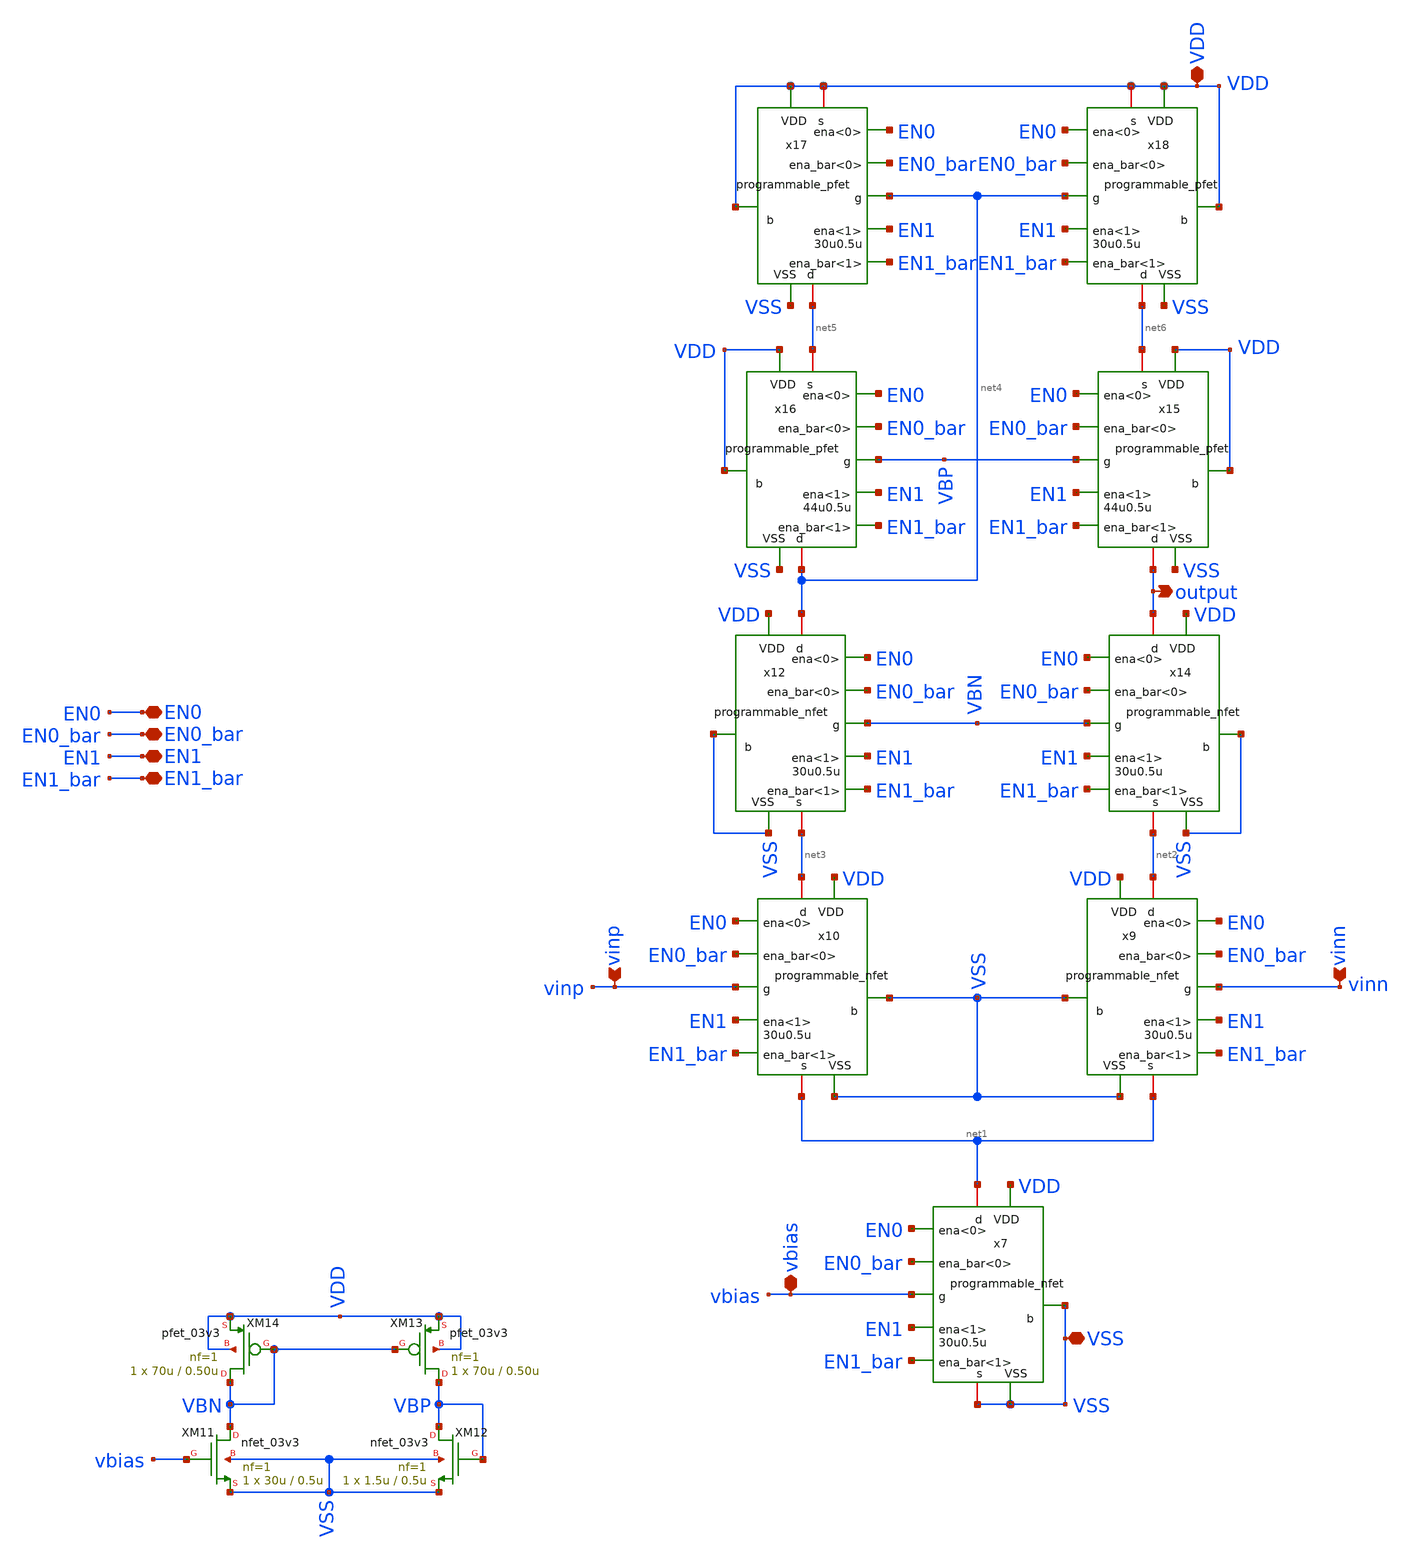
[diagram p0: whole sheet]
** sch_path: designs/libs/core_amps/ota_telescopic/programmable_telescopic_cascode.sch
**.subckt programmable_telescopic_cascode output VDD EN0_bar EN1 EN0 EN1_bar vinp vinn VSS vbias
*.opin output
*.iopin VDD
*.iopin EN0_bar
*.iopin EN1
*.iopin EN0
*.iopin EN1_bar
*.ipin vinp
*.ipin vinn
*.iopin VSS
*.iopin vbias
x7 net1 VSS vbias VSS EN0_bar VDD EN1_bar EN0 EN1 VSS programmable_nfet width=30u length=0.5u
x9 net2 VSS vinn net1 EN0_bar VDD EN1_bar EN0 EN1 VSS programmable_nfet width=30u length=0.5u
x10 net3 VSS vinp net1 EN0_bar VDD EN1_bar EN0 EN1 VSS programmable_nfet width=30u length=0.5u
x12 net4 VSS VBN net3 EN0_bar VDD EN1_bar EN0 EN1 VSS programmable_nfet width=30u length=0.5u
x14 output VSS VBN net2 EN0_bar VDD EN1_bar EN0 EN1 VSS programmable_nfet width=30u length=0.5u
x15 output VDD VBP net6 EN0_bar VDD EN1_bar EN0 EN1 VSS programmable_pfet width=44u length=0.5u
x16 net4 VDD VBP net5 EN0_bar VDD EN1_bar EN0 EN1 VSS programmable_pfet width=44u length=0.5u
x17 net5 VDD net4 VDD EN0_bar VDD EN1_bar EN0 EN1 VSS programmable_pfet width=30u length=0.5u
x18 net6 VDD net4 VDD EN0_bar VDD EN1_bar EN0 EN1 VSS programmable_pfet width=30u length=0.5u
XM11 VBN vbias VSS VSS nfet_03v3 L=0.5u W=30u nf=1 ad='int((nf+1)/2) * W/nf * 0.18u' as='int((nf+2)/2) * W/nf * 0.18u'
+ pd='2*int((nf+1)/2) * (W/nf + 0.18u)' ps='2*int((nf+2)/2) * (W/nf + 0.18u)' nrd='0.18u / W' nrs='0.18u / W'
+ sa=0 sb=0 sd=0 m=1
XM12 VBP VBP VSS VSS nfet_03v3 L=0.5u W=1.5u nf=1 ad='int((nf+1)/2) * W/nf * 0.18u' as='int((nf+2)/2) * W/nf * 0.18u'
+ pd='2*int((nf+1)/2) * (W/nf + 0.18u)' ps='2*int((nf+2)/2) * (W/nf + 0.18u)' nrd='0.18u / W' nrs='0.18u / W'
+ sa=0 sb=0 sd=0 m=1
XM13 VBP VBN VDD VDD pfet_03v3 L=0.50u W=70u nf=1 ad='int((nf+1)/2) * W/nf * 0.18u' as='int((nf+2)/2) * W/nf * 0.18u'
+ pd='2*int((nf+1)/2) * (W/nf + 0.18u)' ps='2*int((nf+2)/2) * (W/nf + 0.18u)' nrd='0.18u / W' nrs='0.18u / W'
+ sa=0 sb=0 sd=0 m=1
XM14 VBN VBN VDD VDD pfet_03v3 L=0.50u W=70u nf=1 ad='int((nf+1)/2) * W/nf * 0.18u' as='int((nf+2)/2) * W/nf * 0.18u'
+ pd='2*int((nf+1)/2) * (W/nf + 0.18u)' ps='2*int((nf+2)/2) * (W/nf + 0.18u)' nrd='0.18u / W' nrs='0.18u / W'
+ sa=0 sb=0 sd=0 m=1
**** begin user architecture code


.include /foss/pdks/gf180mcuD/libs.tech/ngspice/design.ngspice
.lib /foss/pdks/gf180mcuD/libs.tech/ngspice/sm141064.ngspice typical

**** end user architecture code
**.ends
.end
